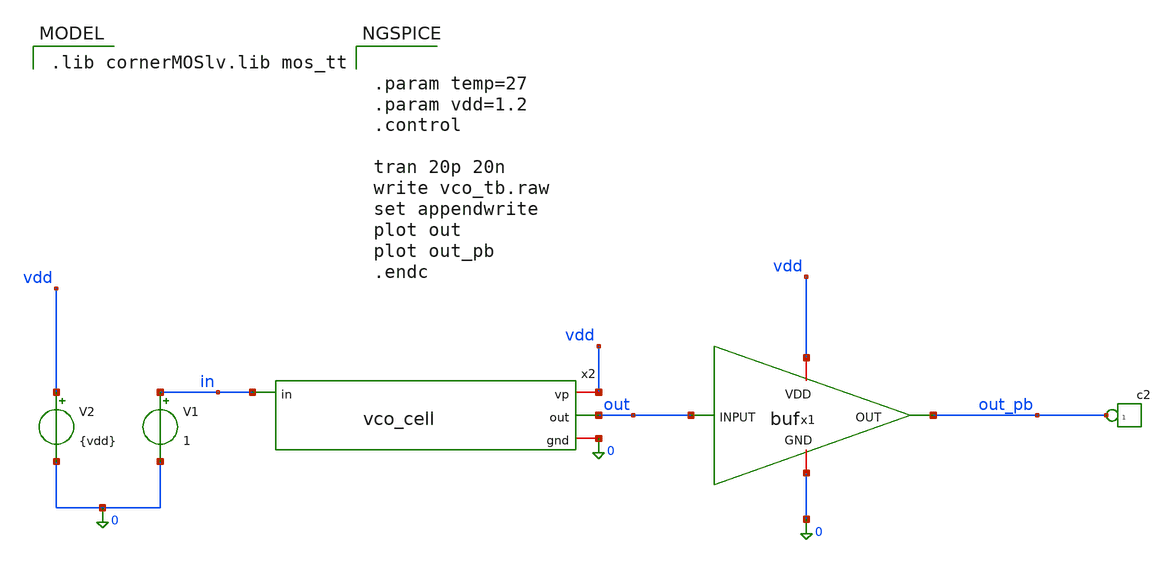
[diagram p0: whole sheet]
** sch_path: schematics/vco/vco_tb/vco_tb_buf.sch
**.subckt vco_tb_buf
x2 vdd out in 0 vco_cell
V1 in 0 1
V2 vdd 0 {vdd}
*connector(1,1) ?1 out_pb
x1 vdd out out_pb 0 buf
**** begin user architecture code


.param temp=27
.param vdd=1.2
.control

tran 20p 20n
write vco_tb.raw
set appendwrite
plot out
plot out_pb
.endc


 .lib cornerMOSlv.lib mos_tt

**** end user architecture code
**.ends

* expanding   symbol:  /foss/designs/CHIP-PLL/vco/vco_cell/vco_cell.sym # of pins=4
** sym_path: schematics/vco/vco_cell/vco_cell.sym
** sch_path: schematics/vco/vco_cell/vco_cell.sch
.subckt vco_cell vp out in gnd
*.ipin in
*.iopin gnd
*.iopin vp
*.opin out
XM1 chwcto in gnd gnd sg13_lv_nmos w=0.405u l=0.420u ng=1 m=1 mm_ok=1
XM2 chwcto chwcto vp vp sg13_lv_pmos w=1.21u l=0.18u ng=1 m=1 mm_ok=1
XM3 1up chwcto vp vp sg13_lv_pmos w=1.21u l=0.18u ng=1 m=1 mm_ok=1
XM4 2up chwcto vp vp sg13_lv_pmos w=1.21u l=0.18u ng=1 m=1 mm_ok=1
XM5 3up chwcto vp vp sg13_lv_pmos w=1.21u l=0.18u ng=1 m=1 mm_ok=1
XM6 4up chwcto vp vp sg13_lv_pmos w=1.21u l=0.18u ng=1 m=1 mm_ok=1
XM7 5up chwcto vp vp sg13_lv_pmos w=1.21u l=0.18u ng=1 m=1 mm_ok=1
XM8 1-2 out 1up 1up sg13_lv_pmos w=1.2u l=0.18u ng=1 m=1 mm_ok=1
XM9 2-3 1-2 2up 2up sg13_lv_pmos w=1.2u l=0.18u ng=1 m=1 mm_ok=1
XM10 3-4 2-3 3up 3up sg13_lv_pmos w=1.2u l=0.18u ng=1 m=1 mm_ok=1
XM11 4-5 3-4 4up 4up sg13_lv_pmos w=1.2u l=0.18u ng=1 m=1 mm_ok=1
XM12 out 4-5 5up 5up sg13_lv_pmos w=1.2u l=0.18u ng=1 m=1 mm_ok=1
XM13 1-2 out 1dn 1dn sg13_lv_nmos w=0.4u l=0.18u ng=1 m=1 mm_ok=1
XM14 2-3 1-2 2dn 2dn sg13_lv_nmos w=0.4u l=0.18u ng=1 m=1 mm_ok=1
XM15 3-4 2-3 3dn 3dn sg13_lv_nmos w=0.4u l=0.18u ng=1 m=1 mm_ok=1
XM16 4-5 3-4 4dn 4dn sg13_lv_nmos w=0.4u l=0.18u ng=1 m=1 mm_ok=1
XM17 out 4-5 5dn 5dn sg13_lv_nmos w=0.4u l=0.18u ng=1 m=1 mm_ok=1
XM18 1dn in gnd gnd sg13_lv_nmos w=0.405u l=0.420u ng=1 m=1 mm_ok=1
XM19 2dn in gnd gnd sg13_lv_nmos w=0.405u l=0.420u ng=1 m=1 mm_ok=1
XM20 3dn in gnd gnd sg13_lv_nmos w=0.405u l=0.420u ng=1 m=1 mm_ok=1
XM21 4dn in gnd gnd sg13_lv_nmos w=0.405u l=0.420u ng=1 m=1 mm_ok=1
XM22 5dn in gnd gnd sg13_lv_nmos w=0.405u l=0.420u ng=1 m=1 mm_ok=1
.ends


* expanding   symbol:  /foss/designs/CHIP-PLL/buf/buf.sym # of pins=4
** sym_path: schematics/buf/buf.sym
** sch_path: schematics/buf/buf.sch
.subckt buf VDD INPUT OUT GND
*.ipin INPUT
*.iopin VDD
*.iopin GND
*.opin OUT
XM9 OUT net3 VDD VDD sg13_hv_pmos w=10u l=0.4u ng=1 m=4 mm_ok=1
XM6 net3 net2 VDD VDD sg13_hv_pmos w=10u l=0.4u ng=1 m=2 mm_ok=1
XM4 net2 net1 VDD VDD sg13_hv_pmos w=10u l=0.4u ng=1 m=1 mm_ok=1
XM2 net1 INPUT VDD VDD sg13_hv_pmos w=5u l=0.4u ng=1 m=1 mm_ok=1
XM1 OUT net3 GND GND sg13_hv_nmos w=10u l=0.45u ng=1 m=4 mm_ok=1
XM3 net3 net2 GND GND sg13_hv_nmos w=10u l=0.45u ng=1 m=2 mm_ok=1
XM5 net2 net1 GND GND sg13_hv_nmos w=10u l=0.45u ng=1 m=1 mm_ok=1
XM7 net1 INPUT GND GND sg13_hv_nmos w=5u l=0.45u ng=1 m=1 mm_ok=1
.ends

.end
